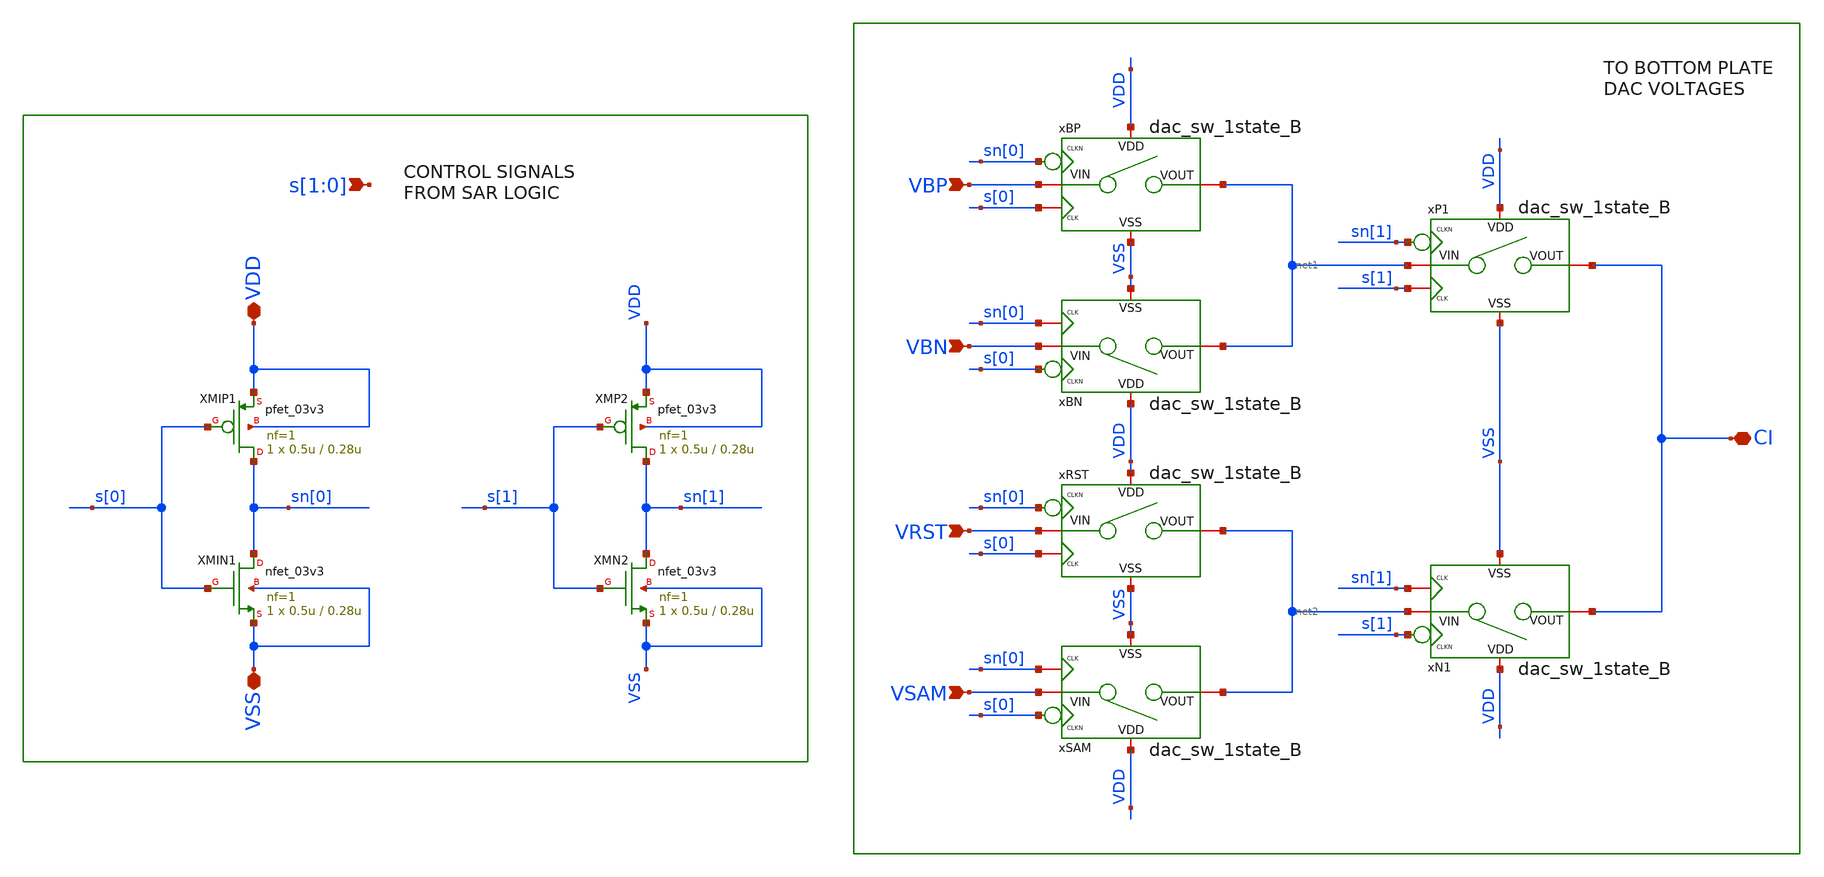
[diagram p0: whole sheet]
** sch_path: designs/sar_adc/dac/analog_mux_4state/xschem/analog_mux_4state.sch
**.subckt analog_mux_4state s[1],s[0] VDD VSS VRST CI VSAM VBP VBN
*.ipin s[1],s[0]
*.iopin VDD
*.iopin VSS
*.ipin VRST
*.iopin CI
*.ipin VSAM
*.ipin VBP
*.ipin VBN
XMIN1 sn[0] s[0] VSS VSS nfet_03v3 L=0.28u W=0.5u nf=1 ad='int((nf+1)/2) * W/nf * 0.18u' as='int((nf+2)/2) * W/nf * 0.18u'
+ pd='2*int((nf+1)/2) * (W/nf + 0.18u)' ps='2*int((nf+2)/2) * (W/nf + 0.18u)' nrd='0.18u / W' nrs='0.18u / W'
+ sa=0 sb=0 sd=0 m=1
XMIP1 sn[0] s[0] VDD VDD pfet_03v3 L=0.28u W=0.5u nf=1 ad='int((nf+1)/2) * W/nf * 0.18u' as='int((nf+2)/2) * W/nf * 0.18u'
+ pd='2*int((nf+1)/2) * (W/nf + 0.18u)' ps='2*int((nf+2)/2) * (W/nf + 0.18u)' nrd='0.18u / W' nrs='0.18u / W'
+ sa=0 sb=0 sd=0 m=1
XMN2 sn[1] s[1] VSS VSS nfet_03v3 L=0.28u W=0.5u nf=1 ad='int((nf+1)/2) * W/nf * 0.18u' as='int((nf+2)/2) * W/nf * 0.18u'
+ pd='2*int((nf+1)/2) * (W/nf + 0.18u)' ps='2*int((nf+2)/2) * (W/nf + 0.18u)' nrd='0.18u / W' nrs='0.18u / W'
+ sa=0 sb=0 sd=0 m=1
XMP2 sn[1] s[1] VDD VDD pfet_03v3 L=0.28u W=0.5u nf=1 ad='int((nf+1)/2) * W/nf * 0.18u' as='int((nf+2)/2) * W/nf * 0.18u'
+ pd='2*int((nf+1)/2) * (W/nf + 0.18u)' ps='2*int((nf+2)/2) * (W/nf + 0.18u)' nrd='0.18u / W' nrs='0.18u / W'
+ sa=0 sb=0 sd=0 m=1
xP1 VDD VSS s[1] net1 CI sn[1] dac_sw_1state_B
xN1 VDD VSS sn[1] net2 CI s[1] dac_sw_1state_B
xBP VDD VSS s[0] VBP net1 sn[0] dac_sw_1state_B
xBN VDD VSS sn[0] VBN net1 s[0] dac_sw_1state_B
xRST VDD VSS s[0] VRST net2 sn[0] dac_sw_1state_B
xSAM VDD VSS sn[0] VSAM net2 s[0] dac_sw_1state_B
**.ends

* expanding   symbol:  designs/sar_adc/dac/dac_sw_1state_B/xschem/dac_sw_1state_B.sym # of pins=6
** sym_path: designs/sar_adc/dac/dac_sw_1state_B/xschem/dac_sw_1state_B.sym
** sch_path: designs/sar_adc/dac/dac_sw_1state_B/xschem/dac_sw_1state_B.sch
.subckt dac_sw_1state_B VDD VSS CLK VIN VOUT CLKN
*.iopin VIN
*.iopin VOUT
*.iopin CLK
*.iopin CLKN
*.iopin VSS
*.iopin VDD
XMSN VOUT CLK VIN VSS nfet_03v3 L=0.28u W=0.5u nf=1 ad='int((nf+1)/2) * W/nf * 0.18u' as='int((nf+2)/2) * W/nf * 0.18u'
+ pd='2*int((nf+1)/2) * (W/nf + 0.18u)' ps='2*int((nf+2)/2) * (W/nf + 0.18u)' nrd='0.18u / W' nrs='0.18u / W'
+ sa=0 sb=0 sd=0 m=10
XMSP VIN CLKN VOUT VDD pfet_03v3 L=0.28u W=0.5u nf=1 ad='int((nf+1)/2) * W/nf * 0.18u' as='int((nf+2)/2) * W/nf * 0.18u'
+ pd='2*int((nf+1)/2) * (W/nf + 0.18u)' ps='2*int((nf+2)/2) * (W/nf + 0.18u)' nrd='0.18u / W' nrs='0.18u / W'
+ sa=0 sb=0 sd=0 m=10
.ends

.end
